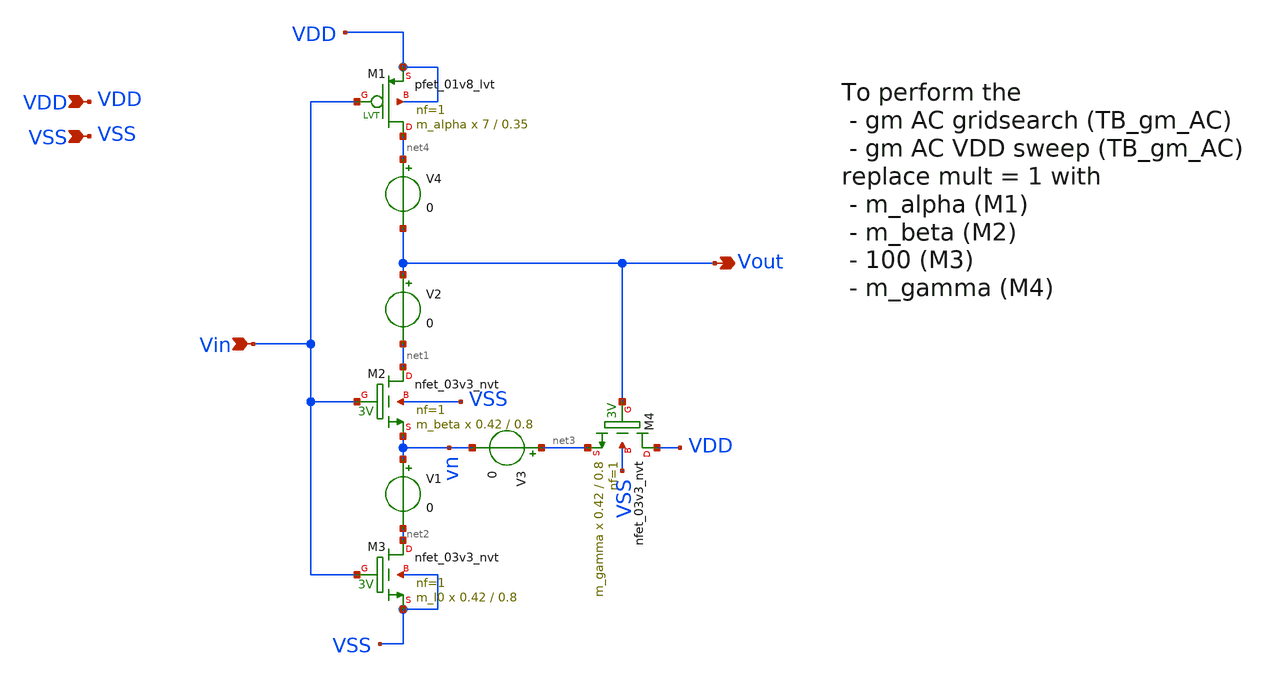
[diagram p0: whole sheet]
** sch_path: design/THESIS_EXP_RO_INVERTER_SKY130A/INV_NVT_feedback.sch
**.subckt INV_NVT_feedback VSS Vin Vout VDD
*.ipin VSS
*.ipin Vin
*.opin Vout
*.ipin VDD
XM1 net4 Vin VDD VDD sky130_fd_pr__pfet_01v8_lvt L=0.35 W=7 nf=1 ad='int((nf+1)/2) * W/nf * 0.29' as='int((nf+2)/2) * W/nf * 0.29'
+ pd='2*int((nf+1)/2) * (W/nf + 0.29)' ps='2*int((nf+2)/2) * (W/nf + 0.29)' nrd='0.29 / W' nrs='0.29 / W'
+ sa=0 sb=0 sd=0 mult=m_alpha m=m_alpha
XM2 net1 Vin vn VSS sky130_fd_pr__nfet_03v3_nvt L=0.8 W=0.42 nf=1 ad='int((nf+1)/2) * W/nf * 0.29' as='int((nf+2)/2) * W/nf * 0.29'
+ pd='2*int((nf+1)/2) * (W/nf + 0.29)' ps='2*int((nf+2)/2) * (W/nf + 0.29)' nrd='0.29 / W' nrs='0.29 / W'
+ sa=0 sb=0 sd=0 mult=m_beta m=m_beta
XM3 net2 Vin VSS VSS sky130_fd_pr__nfet_03v3_nvt L=0.8 W=0.42 nf=1 ad='int((nf+1)/2) * W/nf * 0.29' as='int((nf+2)/2) * W/nf * 0.29'
+ pd='2*int((nf+1)/2) * (W/nf + 0.29)' ps='2*int((nf+2)/2) * (W/nf + 0.29)' nrd='0.29 / W' nrs='0.29 / W'
+ sa=0 sb=0 sd=0 mult=m_I0 m=m_I0
XM4 VDD Vout net3 VSS sky130_fd_pr__nfet_03v3_nvt L=0.8 W=0.42 nf=1 ad='int((nf+1)/2) * W/nf * 0.29'
+ as='int((nf+2)/2) * W/nf * 0.29' pd='2*int((nf+1)/2) * (W/nf + 0.29)' ps='2*int((nf+2)/2) * (W/nf + 0.29)'
+ nrd='0.29 / W' nrs='0.29 / W' sa=0 sb=0 sd=0 mult=m_gamma m=m_gamma
V1 vn net2 0
.save i(v1)
V2 Vout net1 0
.save i(v2)
V3 net3 vn 0
.save i(v3)
V4 net4 Vout 0
.save i(v4)
**.ends
.end
